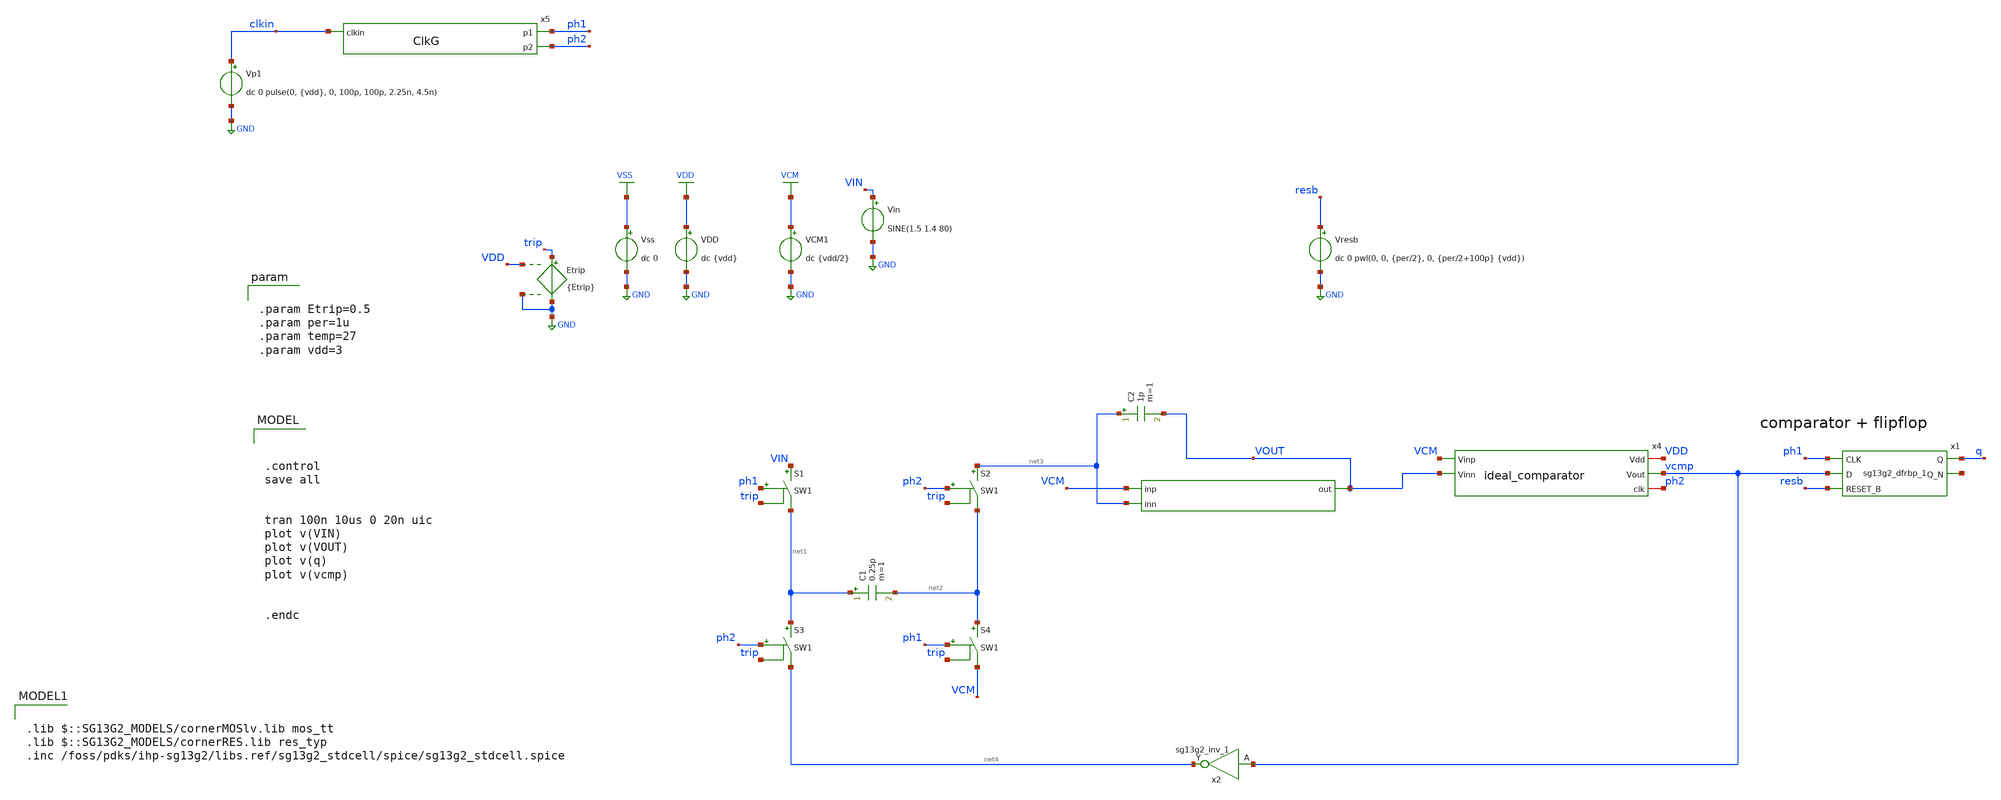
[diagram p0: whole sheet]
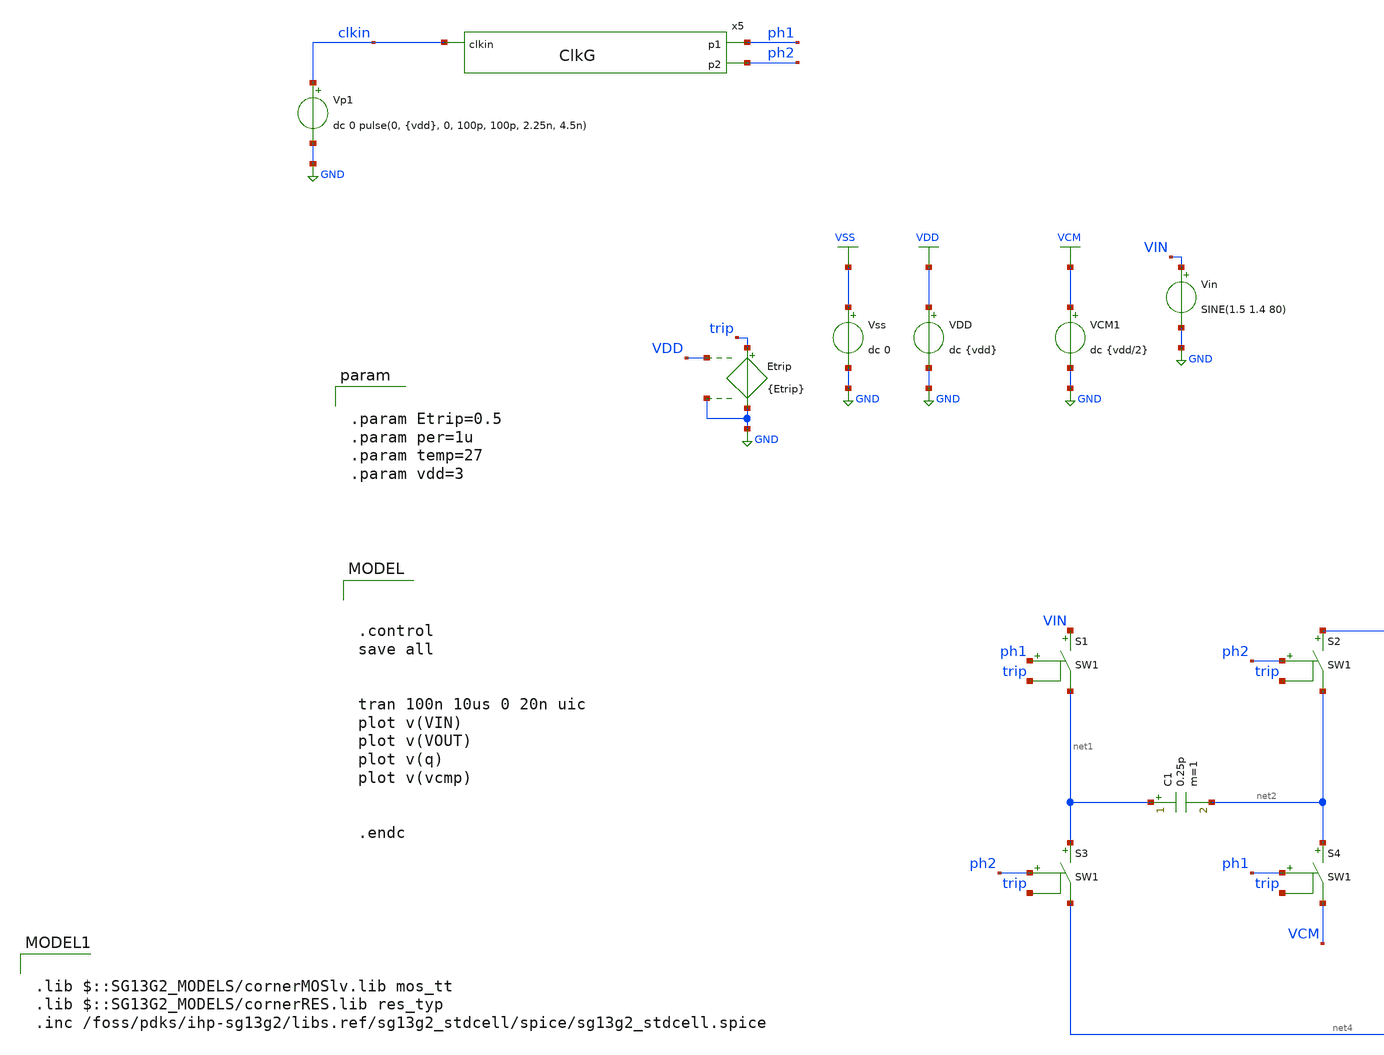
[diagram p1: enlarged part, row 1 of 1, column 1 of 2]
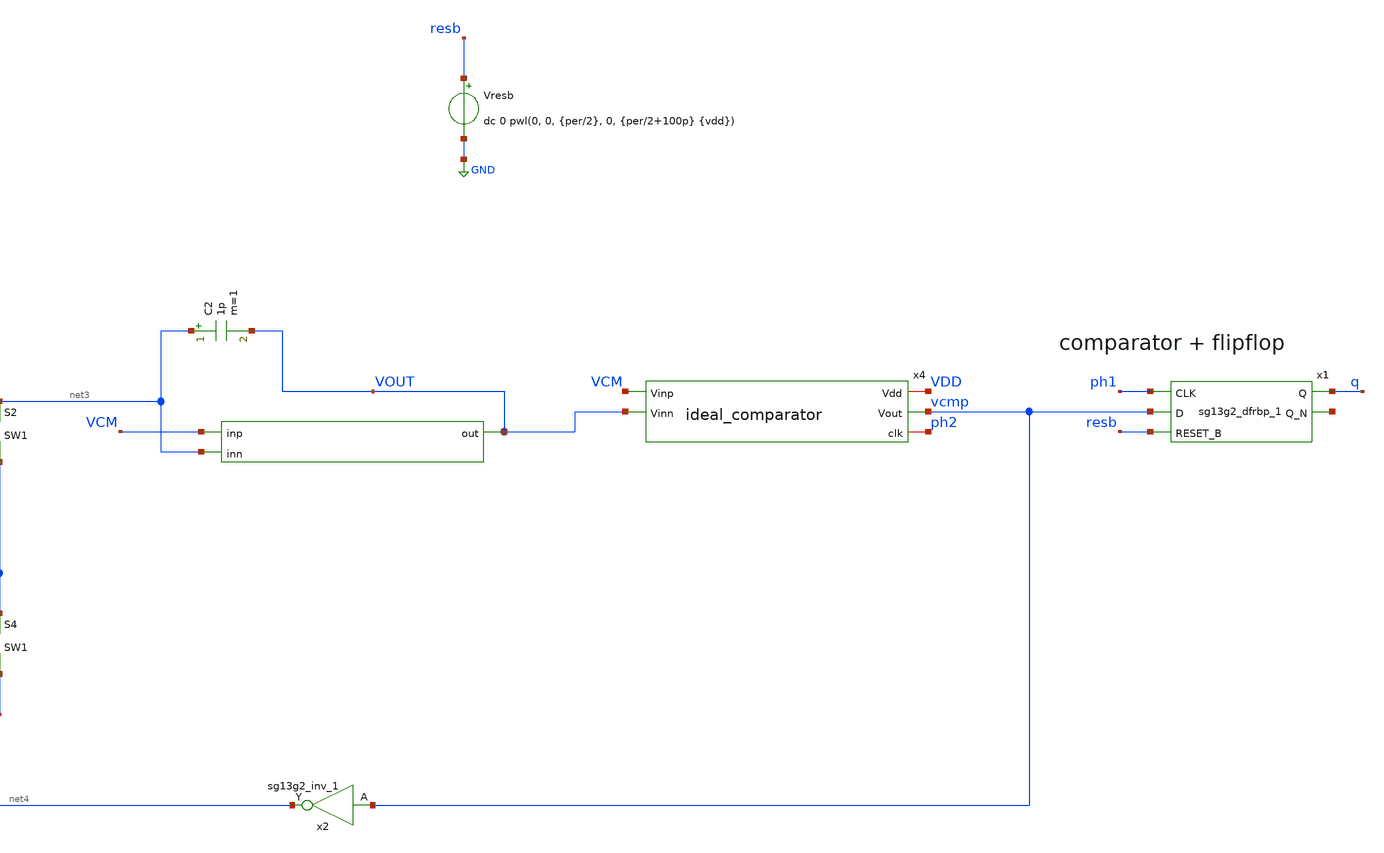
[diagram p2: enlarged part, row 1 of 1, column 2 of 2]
** sch_path: DSM_1storder/Schematic_Level/xschem/DSM_with_clock.sch
**.subckt DSM_with_clock
C1 net1 net2 0.25p m=1
S2 net3 net2 ph2 trip SW1
S3 net1 net4 ph2 trip SW1
S4 net2 VCM ph1 trip SW1
VDD VDD GND dc {vdd}
VCM1 VCM GND dc {vdd/2}
C2 net3 VOUT 1p m=1
x1 q net5 ph1 vcmp resb VDD VSS sg13g2_dfrbp_1
Vresb resb GND dc 0 pwl(0, 0, {per/2}, 0, {per/2+100p} {vdd})
x2 net4 vcmp 1.5 0 sg13g2_inv_1
x3 VOUT VCM net3 ideal_opamp
x4 VDD vcmp VCM ph2 VOUT ideal_comparator
S1 VIN net1 ph1 trip SW1
Etrip trip GND VDD GND {Etrip}
Vin VIN GND SINE(1.5 1.4 80)
x5 clkin ph1 ph2 ClkG
Vss VSS GND dc 0
Vp1 clkin GND dc 0 pulse(0, {vdd}, 0, 100p, 100p, 2.25n, 4.5n)
**** begin user architecture code



.control
save all


tran 100n 10us 0 20n uic
plot v(VIN)
plot v(VOUT)
plot v(q)
plot v(vcmp)


.endc



.lib $::SG13G2_MODELS/cornerMOSlv.lib mos_tt
.lib $::SG13G2_MODELS/cornerRES.lib res_typ
.inc /foss/pdks/ihp-sg13g2/libs.ref/sg13g2_stdcell/spice/sg13g2_stdcell.spice



.param Etrip=0.5
.param per=1u
.param temp=27
.param vdd=3


**** end user architecture code
**.ends
.GLOBAL GND
.GLOBAL VDD
.GLOBAL VCM
.GLOBAL VSS
**** begin user architecture code
.MODEL SW1 SW(VT=0.5 VH=0 RON=0.1 ROFF=100M)
**** end user architecture code
.end
